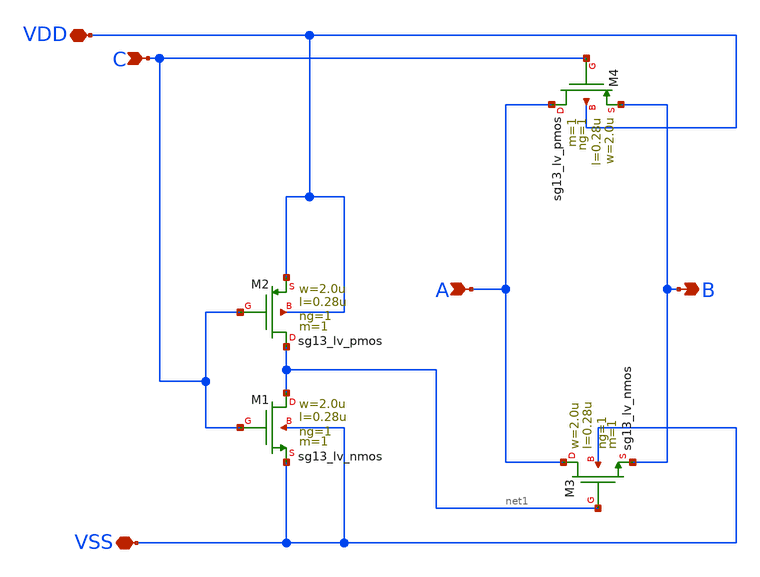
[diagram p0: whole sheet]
** sch_path: blocks/composite/dpi_adexp_neuron/design_data/xschem/tgf.sch
**.subckt tgf A B C VDD VSS
*.ipin A
*.opin B
*.ipin C
*.iopin VDD
*.iopin VSS
XM1 net1 C VSS VSS sg13_lv_nmos w=2.0u l=0.28u ng=1 m=1 mm_ok=1
XM2 net1 C VDD VDD sg13_lv_pmos w=2.0u l=0.28u ng=1 m=1 mm_ok=1
XM3 A net1 B VSS sg13_lv_nmos w=2.0u l=0.28u ng=1 m=1 mm_ok=1
XM4 A C B VDD sg13_lv_pmos w=2.0u l=0.28u ng=1 m=1 mm_ok=1
**.ends
.end
